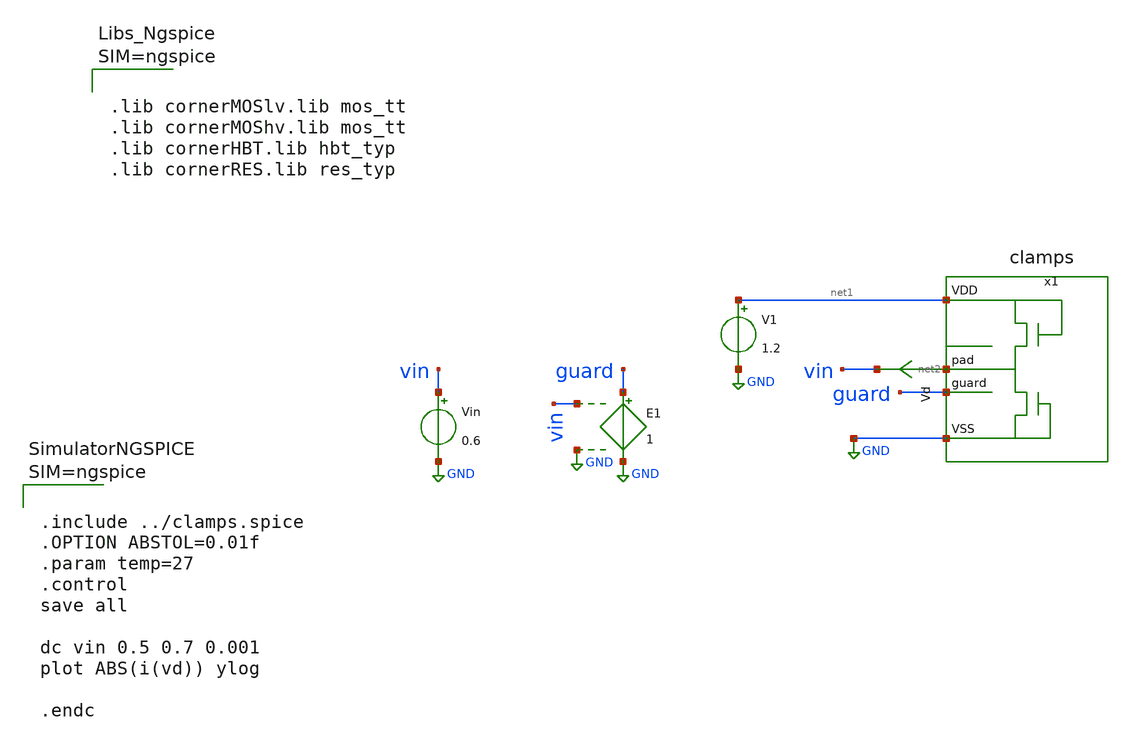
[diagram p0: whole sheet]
** sch_path: trident_test_structures/design_data/xschem/IOPadAnalog_submodules/clamps_tb.sch
**.subckt clamps_tb
Vd net2 vin 0
.save i(vd)
Vin vin GND 0.6
V1 net1 GND 1.2
E1 guard GND vin GND 1
x1 net1 net2 guard GND clamps
**** begin user architecture code



.lib cornerMOSlv.lib mos_tt
.lib cornerMOShv.lib mos_tt
.lib cornerHBT.lib hbt_typ
.lib cornerRES.lib res_typ







.include ../clamps.spice
.OPTION ABSTOL=0.01f
.param temp=27
.control
save all

dc vin 0.5 0.7 0.001
plot ABS(i(vd)) ylog

.endc



**** end user architecture code
**.ends
.GLOBAL GND
.end
